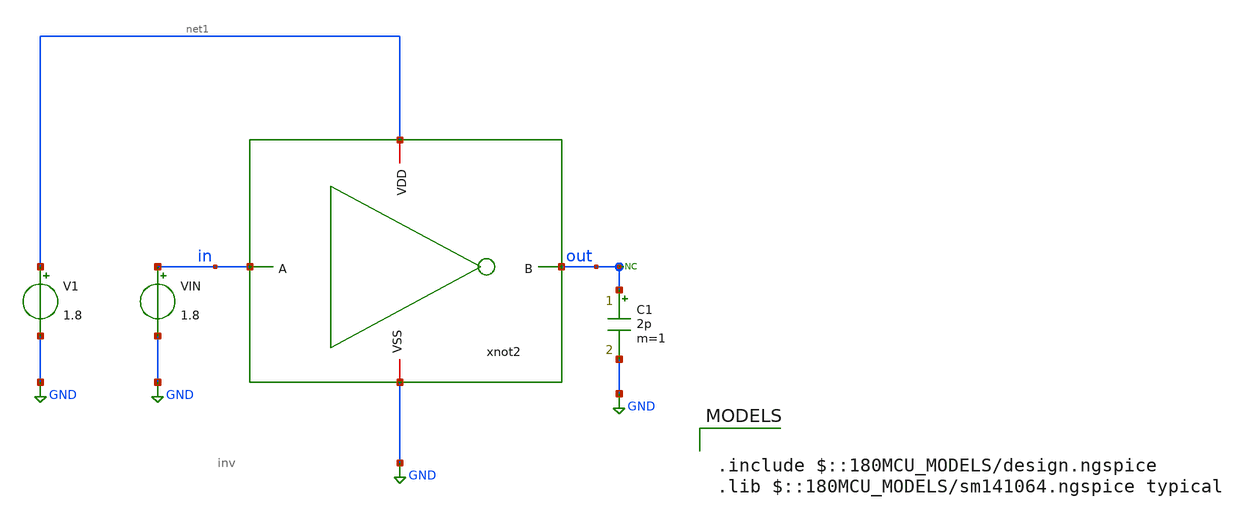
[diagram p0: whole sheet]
** sch_path: designs/ring_oscillator_pg/inverter/inv_prue.sch
**.subckt inv_prue
V1 net1 GND 1.8
VIN in GND 1.8
* noconn out
C1 out GND 2p m=1
xnot2 net1 in out GND inv
**** begin user architecture code

.include $::180MCU_MODELS/design.ngspice
.lib $::180MCU_MODELS/sm141064.ngspice typical



.control
save all

** Define input signal
let fsig = 1k
let tper = 1/fsig
let tfr = 0.01*tper
let ton = 0.5*tper-2*tfr

** Define transient params
let tstop = 2*tper
let tstep = 0.001*tper

print tper tstop tstep

** Set Sources
alter @VIN[DC] = 0.0
alter @VIN[PULSE] = [ 0 1.8 0 $&tfr $&tfr $&ton  $&tper 0 ]

** Simulations
op
dc vin 0 1.8 0.01
tran $&tstep $&tstop

let VP=1.8
let per10 = Vp*0.1
let per50 = Vp*0.5
let per90 = Vp*0.9

meas TRAN t_rise  TRIG v(out) VAL=per10 rise=2  TARG v(out) VAL=per90 rise=2
meas TRAN t_fall  TRIG v(out) VAL=per90 fall=2  TARG v(out) VAL=per10 fall=2
meas TRAN t_delay  TRIG v(in) VAL=per50 rise=1 TARG v(out) VAL=per50 fall=1
meas TRAN T_period TRIG v(out) VAL=per50 rise=2 TARG v(out) VAL=per50 rise=3
let F_recu=1/T_period

echo '==============TRAN measurements========='

print t_delay
print t_rise
print t_fall
print T_period
print F_recu
print T_period/2


** Plots
setplot dc1
let vout = v(out)
plot vout

setplot tran1
let vout = v(out)
let vin = v(in)
let ivdd = -v1#branch*1e
plot vout vin ivdd

setplot op1

write inv_tb.raw
.endc


**** end user architecture code
**.ends

* expanding   symbol:  gf180/ring_oscillator_pg/inverter/inv.sym # of pins=4
** sym_path: designs/ring_oscillator_pg/inverter/inv.sym
** sch_path: designs/ring_oscillator_pg/inverter/inv.sch
.subckt inv VDD A B VSS
*.iopin VSS
*.iopin B
*.iopin A
*.iopin VDD
XM1 B A VDD VDD pfet_03v3 L=0.28u W=100u nf=1 ad='int((nf+1)/2) * W/nf * 0.18u' as='int((nf+2)/2) * W/nf * 0.18u'
+ pd='2*int((nf+1)/2) * (W/nf + 0.18u)' ps='2*int((nf+2)/2) * (W/nf + 0.18u)' nrd='0.18u / W' nrs='0.18u / W'
+ sa=0 sb=0 sd=0 m=4
XM2 B A VSS VSS nfet_03v3 L=0.28u W=100u nf=1 ad='int((nf+1)/2) * W/nf * 0.18u' as='int((nf+2)/2) * W/nf * 0.18u'
+ pd='2*int((nf+1)/2) * (W/nf + 0.18u)' ps='2*int((nf+2)/2) * (W/nf + 0.18u)' nrd='0.18u / W' nrs='0.18u / W'
+ sa=0 sb=0 sd=0 m=2
.ends

.GLOBAL GND
.end
